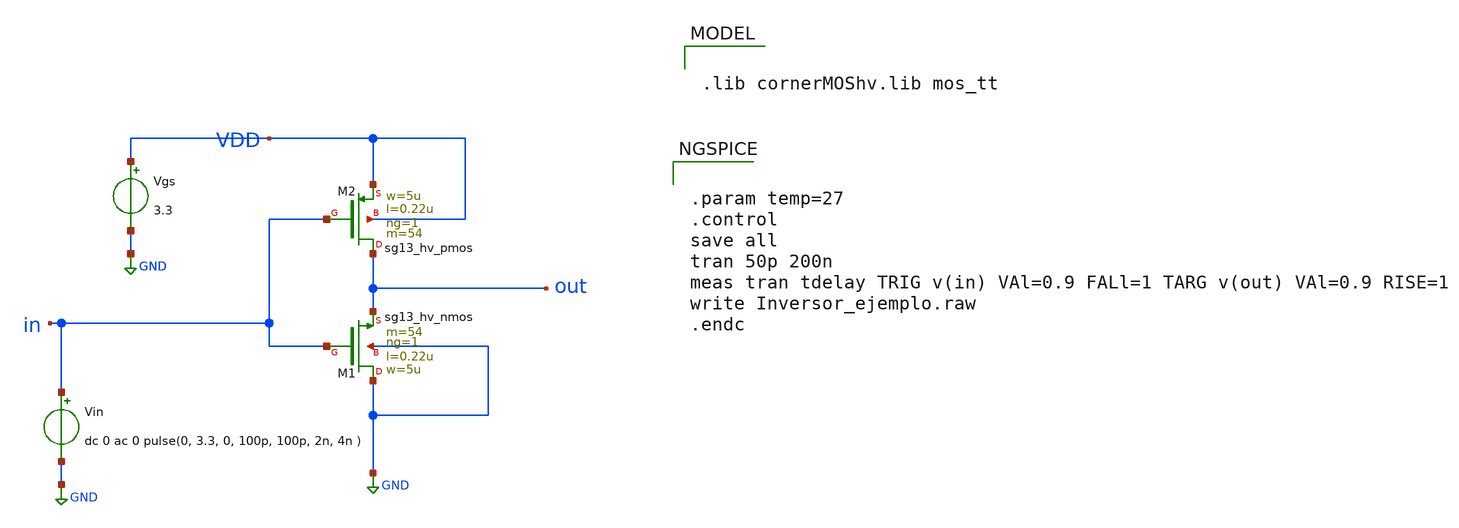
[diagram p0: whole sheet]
** sch_path: klayout/Inversor_ejemplo.sch
**.subckt Inversor_ejemplo
XM1 GND in out GND sg13_hv_nmos w=5u l=0.22u ng=1 m=54 mm_ok=1
XM2 out in VDD VDD sg13_hv_pmos w=5u l=0.22u ng=1 m=54 mm_ok=1
Vgs VDD GND 3.3
Vin in GND dc 0 ac 0 pulse(0, 3.3, 0, 100p, 100p, 2n, 4n )
**** begin user architecture code

.lib cornerMOShv.lib mos_tt



.param temp=27
.control
save all
tran 50p 200n
meas tran tdelay TRIG v(in) VAl=0.9 FALl=1 TARG v(out) VAl=0.9 RISE=1
write Inversor_ejemplo.raw
.endc


**** end user architecture code
**.ends
.GLOBAL GND
.end
